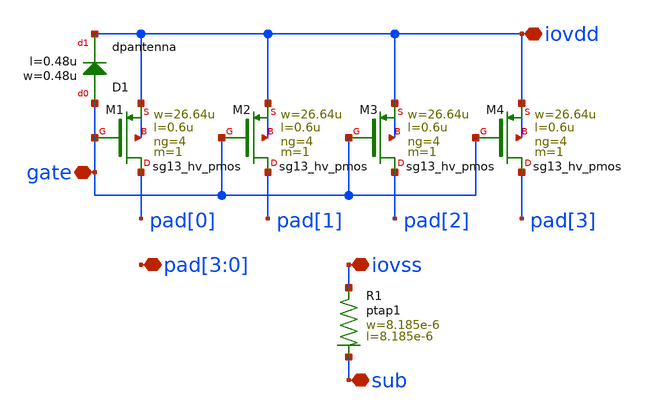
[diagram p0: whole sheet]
** sch_path: MSPHY6034-main/dependencies/unic_cass_2025_team04_padring/xschem/openpdk-libraries/ihp-sg13g2/sg13g2_io/xschem/sg13g2_Clamp_P8N8D.sch
**.subckt sg13g2_Clamp_P8N8D iovss gate iovdd pad[3],pad[2],pad[1],pad[0] sub
*.iopin iovss
*.iopin gate
*.iopin iovdd
*.iopin pad[3],pad[2],pad[1],pad[0]
*.iopin sub
XR1 iovss sub ptap1 R=9.826 w=8.185e-6 l=8.185e-6
XM1 pad[0] gate iovdd iovdd sg13_hv_pmos w=26.64u l=0.6u ng=4 m=1 mm_ok=1
XD1 gate iovdd dpantenna l=0.48u w=0.48u
XM2 pad[1] gate iovdd iovdd sg13_hv_pmos w=26.64u l=0.6u ng=4 m=1 mm_ok=1
XM3 pad[2] gate iovdd iovdd sg13_hv_pmos w=26.64u l=0.6u ng=4 m=1 mm_ok=1
XM4 pad[3] gate iovdd iovdd sg13_hv_pmos w=26.64u l=0.6u ng=4 m=1 mm_ok=1
**.ends
.end
